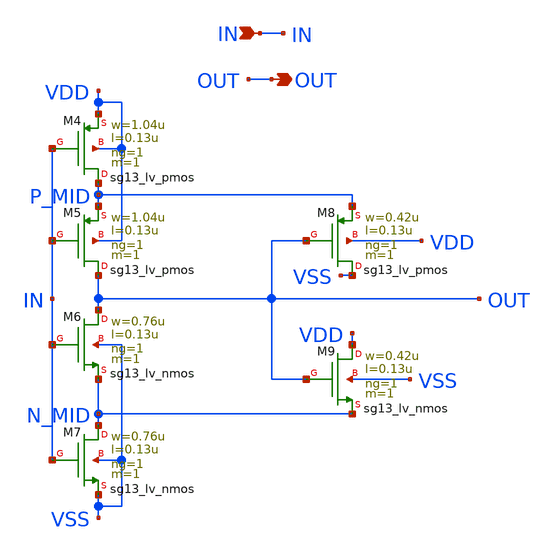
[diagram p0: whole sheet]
** sch_path: design/blocks/schmitt/schematic/schmitt.sch
**.subckt schmitt OUT IN
*.opin OUT
*.ipin IN
XM4 P_MID IN VDD VDD sg13_lv_pmos w=1.04u l=0.13u ng=1 m=1 mm_ok=1
XM6 OUT IN N_MID VSS sg13_lv_nmos w=0.76u l=0.13u ng=1 m=1 mm_ok=1
XM5 OUT IN P_MID VDD sg13_lv_pmos w=1.04u l=0.13u ng=1 m=1 mm_ok=1
XM7 N_MID IN VSS VSS sg13_lv_nmos w=0.76u l=0.13u ng=1 m=1 mm_ok=1
XM8 VSS OUT P_MID VDD sg13_lv_pmos w=0.42u l=0.13u ng=1 m=1 mm_ok=1
XM9 VDD OUT N_MID VSS sg13_lv_nmos w=0.42u l=0.13u ng=1 m=1 mm_ok=1
**.ends
.end
